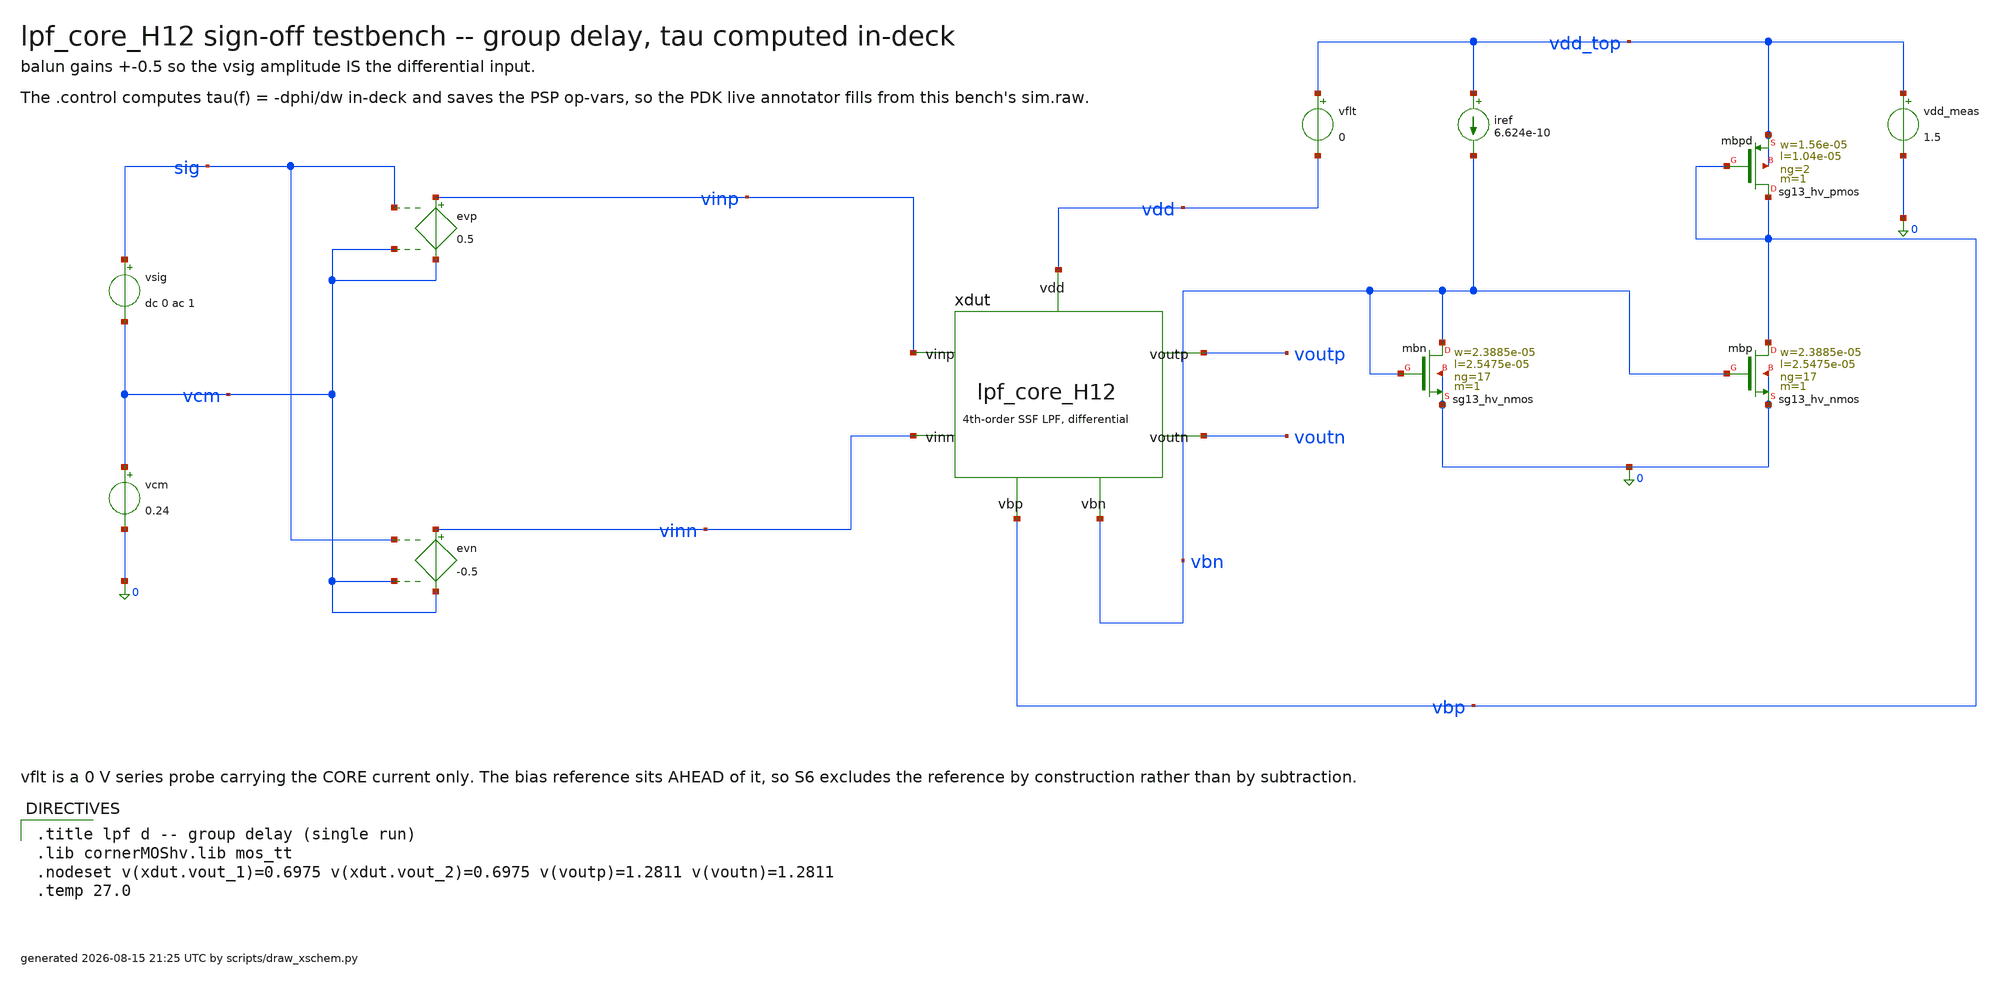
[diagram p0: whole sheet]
** sch_path: signoff/post-pvt/H12-robust/lpf_tb_H12_gd.sch
**.subckt lpf_tb_H12_gd
vsig sig vcm dc 0 ac 1
vcm vcm 0 0.24
evp vinp vcm sig vcm 0.5
evn vinn vcm sig vcm -0.5
xdut vinp vinn voutp voutn vbn vbp vdd lpf_core_H12
vflt vdd_top vdd 0
vdd_meas vdd_top 0 1.5
iref vdd_top vbn 6.624e-10
Xmbn vbn vbn 0 0 sg13_hv_nmos w=2.3885e-05 l=2.5475e-05 ng=17 m=1 mm_ok=1
Xmbp vbp vbn 0 0 sg13_hv_nmos w=2.3885e-05 l=2.5475e-05 ng=17 m=1 mm_ok=1
Xmbpd vbp vbp vdd_top vdd_top sg13_hv_pmos w=1.56e-05 l=1.04e-05 ng=2 m=1 mm_ok=1
**** begin user architecture code

.title lpf d -- group delay (single run)
.lib cornerMOShv.lib mos_tt
.nodeset v(xdut.vout_1)=0.6975 v(xdut.vout_2)=0.6975 v(voutp)=1.2811 v(voutn)=1.2811
.temp 27.0


.control
set filetype=binary
set appendwrite
save all @n.xdut.xm2.nsg13_hv_pmos[ids] @n.xdut.xm2.nsg13_hv_pmos[gm] @n.xdut.xm2.nsg13_hv_pmos[gds]
+ @n.xdut.xm2.nsg13_hv_pmos[gmb] @n.xdut.xm2.nsg13_hv_pmos[vgs] @n.xdut.xm2.nsg13_hv_pmos[vds] @n.xdut.xm2.nsg13_hv_pmos[vth]
+ @n.xdut.xm2.nsg13_hv_pmos[vdss] @n.xdut.xm2.nsg13_hv_pmos[cgg] @n.xdut.xm5.nsg13_hv_pmos[ids] @n.xdut.xm5.nsg13_hv_pmos[gm]
+ @n.xdut.xm5.nsg13_hv_pmos[gds] @n.xdut.xm5.nsg13_hv_pmos[gmb] @n.xdut.xm5.nsg13_hv_pmos[vgs] @n.xdut.xm5.nsg13_hv_pmos[vds]
+ @n.xdut.xm5.nsg13_hv_pmos[vth] @n.xdut.xm5.nsg13_hv_pmos[vdss] @n.xdut.xm5.nsg13_hv_pmos[cgg] @n.xdut.xm4.nsg13_hv_nmos[ids]
+ @n.xdut.xm4.nsg13_hv_nmos[gm] @n.xdut.xm4.nsg13_hv_nmos[gds] @n.xdut.xm4.nsg13_hv_nmos[gmb] @n.xdut.xm4.nsg13_hv_nmos[vgs]
+ @n.xdut.xm4.nsg13_hv_nmos[vds] @n.xdut.xm4.nsg13_hv_nmos[vth] @n.xdut.xm4.nsg13_hv_nmos[vdss] @n.xdut.xm4.nsg13_hv_nmos[cgg]
+ @n.xdut.xm8.nsg13_hv_nmos[ids] @n.xdut.xm8.nsg13_hv_nmos[gm] @n.xdut.xm8.nsg13_hv_nmos[gds] @n.xdut.xm8.nsg13_hv_nmos[gmb]
+ @n.xdut.xm8.nsg13_hv_nmos[vgs] @n.xdut.xm8.nsg13_hv_nmos[vds] @n.xdut.xm8.nsg13_hv_nmos[vth] @n.xdut.xm8.nsg13_hv_nmos[vdss]
+ @n.xdut.xm8.nsg13_hv_nmos[cgg] @n.xdut.xm9.nsg13_hv_nmos[ids] @n.xdut.xm9.nsg13_hv_nmos[gm] @n.xdut.xm9.nsg13_hv_nmos[gds]
+ @n.xdut.xm9.nsg13_hv_nmos[gmb] @n.xdut.xm9.nsg13_hv_nmos[vgs] @n.xdut.xm9.nsg13_hv_nmos[vds] @n.xdut.xm9.nsg13_hv_nmos[vth]
+ @n.xdut.xm9.nsg13_hv_nmos[vdss] @n.xdut.xm9.nsg13_hv_nmos[cgg] @n.xdut.xm10.nsg13_hv_nmos[ids] @n.xdut.xm10.nsg13_hv_nmos[gm]
+ @n.xdut.xm10.nsg13_hv_nmos[gds] @n.xdut.xm10.nsg13_hv_nmos[gmb] @n.xdut.xm10.nsg13_hv_nmos[vgs] @n.xdut.xm10.nsg13_hv_nmos[vds]
+ @n.xdut.xm10.nsg13_hv_nmos[vth] @n.xdut.xm10.nsg13_hv_nmos[vdss] @n.xdut.xm10.nsg13_hv_nmos[cgg] @n.xdut.xmst.nsg13_hv_pmos[ids]
+ @n.xdut.xmst.nsg13_hv_pmos[gm] @n.xdut.xmst.nsg13_hv_pmos[gds] @n.xdut.xmst.nsg13_hv_pmos[gmb] @n.xdut.xmst.nsg13_hv_pmos[vgs]
+ @n.xdut.xmst.nsg13_hv_pmos[vds] @n.xdut.xmst.nsg13_hv_pmos[vth] @n.xdut.xmst.nsg13_hv_pmos[vdss] @n.xdut.xmst.nsg13_hv_pmos[cgg]
+ @n.xdut.xmstn.nsg13_hv_pmos[ids] @n.xdut.xmstn.nsg13_hv_pmos[gm] @n.xdut.xmstn.nsg13_hv_pmos[gds] @n.xdut.xmstn.nsg13_hv_pmos[gmb]
+ @n.xdut.xmstn.nsg13_hv_pmos[vgs] @n.xdut.xmstn.nsg13_hv_pmos[vds] @n.xdut.xmstn.nsg13_hv_pmos[vth] @n.xdut.xmstn.nsg13_hv_pmos[vdss]
+ @n.xdut.xmstn.nsg13_hv_pmos[cgg] @n.xdut.xm0.nsg13_hv_pmos[ids] @n.xdut.xm0.nsg13_hv_pmos[gm] @n.xdut.xm0.nsg13_hv_pmos[gds]
+ @n.xdut.xm0.nsg13_hv_pmos[gmb] @n.xdut.xm0.nsg13_hv_pmos[vgs] @n.xdut.xm0.nsg13_hv_pmos[vds] @n.xdut.xm0.nsg13_hv_pmos[vth]
+ @n.xdut.xm0.nsg13_hv_pmos[vdss] @n.xdut.xm0.nsg13_hv_pmos[cgg] @n.xdut.xm1.nsg13_hv_pmos[ids] @n.xdut.xm1.nsg13_hv_pmos[gm]
+ @n.xdut.xm1.nsg13_hv_pmos[gds] @n.xdut.xm1.nsg13_hv_pmos[gmb] @n.xdut.xm1.nsg13_hv_pmos[vgs] @n.xdut.xm1.nsg13_hv_pmos[vds]
+ @n.xdut.xm1.nsg13_hv_pmos[vth] @n.xdut.xm1.nsg13_hv_pmos[vdss] @n.xdut.xm1.nsg13_hv_pmos[cgg] @n.xdut.xm14.nsg13_hv_pmos[ids]
+ @n.xdut.xm14.nsg13_hv_pmos[gm] @n.xdut.xm14.nsg13_hv_pmos[gds] @n.xdut.xm14.nsg13_hv_pmos[gmb] @n.xdut.xm14.nsg13_hv_pmos[vgs]
+ @n.xdut.xm14.nsg13_hv_pmos[vds] @n.xdut.xm14.nsg13_hv_pmos[vth] @n.xdut.xm14.nsg13_hv_pmos[vdss] @n.xdut.xm14.nsg13_hv_pmos[cgg]
+ @n.xdut.xm15.nsg13_hv_pmos[ids] @n.xdut.xm15.nsg13_hv_pmos[gm] @n.xdut.xm15.nsg13_hv_pmos[gds] @n.xdut.xm15.nsg13_hv_pmos[gmb]
+ @n.xdut.xm15.nsg13_hv_pmos[vgs] @n.xdut.xm15.nsg13_hv_pmos[vds] @n.xdut.xm15.nsg13_hv_pmos[vth] @n.xdut.xm15.nsg13_hv_pmos[vdss]
+ @n.xdut.xm15.nsg13_hv_pmos[cgg] @n.xdut.xr1.nsg13_hv_pmos[ids] @n.xdut.xr1.nsg13_hv_pmos[gm] @n.xdut.xr1.nsg13_hv_pmos[gds]
+ @n.xdut.xr1.nsg13_hv_pmos[gmb] @n.xdut.xr1.nsg13_hv_pmos[vgs] @n.xdut.xr1.nsg13_hv_pmos[vds] @n.xdut.xr1.nsg13_hv_pmos[vth]
+ @n.xdut.xr1.nsg13_hv_pmos[vdss] @n.xdut.xr1.nsg13_hv_pmos[cgg] @n.xdut.xr1.nsg13_hv_pmos[ids] @n.xdut.xr1.nsg13_hv_pmos[gm]
+ @n.xdut.xr1.nsg13_hv_pmos[gds] @n.xdut.xr1.nsg13_hv_pmos[gmb] @n.xdut.xr1.nsg13_hv_pmos[vgs] @n.xdut.xr1.nsg13_hv_pmos[vds]
+ @n.xdut.xr1.nsg13_hv_pmos[vth] @n.xdut.xr1.nsg13_hv_pmos[vdss] @n.xdut.xr1.nsg13_hv_pmos[cgg] @n.xdut.xr2.nsg13_hv_pmos[ids]
+ @n.xdut.xr2.nsg13_hv_pmos[gm] @n.xdut.xr2.nsg13_hv_pmos[gds] @n.xdut.xr2.nsg13_hv_pmos[gmb] @n.xdut.xr2.nsg13_hv_pmos[vgs]
+ @n.xdut.xr2.nsg13_hv_pmos[vds] @n.xdut.xr2.nsg13_hv_pmos[vth] @n.xdut.xr2.nsg13_hv_pmos[vdss] @n.xdut.xr2.nsg13_hv_pmos[cgg]
+ @n.xdut.xr2.nsg13_hv_pmos[ids] @n.xdut.xr2.nsg13_hv_pmos[gm] @n.xdut.xr2.nsg13_hv_pmos[gds] @n.xdut.xr2.nsg13_hv_pmos[gmb]
+ @n.xdut.xr2.nsg13_hv_pmos[vgs] @n.xdut.xr2.nsg13_hv_pmos[vds] @n.xdut.xr2.nsg13_hv_pmos[vth] @n.xdut.xr2.nsg13_hv_pmos[vdss]
+ @n.xdut.xr2.nsg13_hv_pmos[cgg] @n.xdut.xr3.nsg13_hv_nmos[ids] @n.xdut.xr3.nsg13_hv_nmos[gm] @n.xdut.xr3.nsg13_hv_nmos[gds]
+ @n.xdut.xr3.nsg13_hv_nmos[gmb] @n.xdut.xr3.nsg13_hv_nmos[vgs] @n.xdut.xr3.nsg13_hv_nmos[vds] @n.xdut.xr3.nsg13_hv_nmos[vth]
+ @n.xdut.xr3.nsg13_hv_nmos[vdss] @n.xdut.xr3.nsg13_hv_nmos[cgg] @n.xdut.xr3.nsg13_hv_nmos[ids] @n.xdut.xr3.nsg13_hv_nmos[gm]
+ @n.xdut.xr3.nsg13_hv_nmos[gds] @n.xdut.xr3.nsg13_hv_nmos[gmb] @n.xdut.xr3.nsg13_hv_nmos[vgs] @n.xdut.xr3.nsg13_hv_nmos[vds]
+ @n.xdut.xr3.nsg13_hv_nmos[vth] @n.xdut.xr3.nsg13_hv_nmos[vdss] @n.xdut.xr3.nsg13_hv_nmos[cgg]
op
write sim.raw
ac dec 50 0.1 1000
let hdiff = v(voutp) - v(voutn)
let hdb = db(mag(hdiff))
let dc_db = hdb[0]
let ph = cph(hdiff)
let gd = -deriv(ph) / (2 * pi)
let gd_dc_ms = gd[0] * 1e3
let gd_max_ms = vecmax(gd) * 1e3
let hrel = hdb - dc_db
meas ac fc_hz when hrel = -3 fall = 1
print dc_db gd_dc_ms gd_max_ms
write sim.raw hdiff ph gd frequency
.endc

**** end user architecture code
**.ends

* expanding   symbol:  lpf_core_H12.sym # of pins=7
** sym_path: signoff/post-pvt/H12-robust/lpf_core_H12.sym
** sch_path: signoff/post-pvt/H12-robust/lpf_core_H12.sch
.subckt lpf_core_H12 vinp vinn voutp voutn vbn vbp vdd
*.ipin vinp
*.ipin vinn
*.opin voutp
*.opin voutn
*.ipin vdd
*.ipin vbn
*.ipin vbp
Xm2 net2 vinp vout_1 vout_1 sg13_hv_pmos w=1.56e-05 l=1.04e-05 ng=2 m=1 mm_ok=1
Xm5 net3 vinn vout_2 vout_2 sg13_hv_pmos w=1.56e-05 l=1.04e-05 ng=2 m=1 mm_ok=1
Xm4 vout_1 net2 0 0 sg13_hv_nmos w=1.5e-06 l=4.5e-05 ng=1 m=1 mm_ok=1
Xm8 vout_2 net3 0 0 sg13_hv_nmos w=1.5e-06 l=4.5e-05 ng=1 m=1 mm_ok=1
Xm9 net2 vbn 0 0 sg13_hv_nmos w=2.3885e-05 l=2.5475e-05 ng=17 m=1 mm_ok=1
Xm10 net3 vbn 0 0 sg13_hv_nmos w=2.3885e-05 l=2.5475e-05 ng=17 m=1 mm_ok=1
Xmst vout_1 vbr net4 net4 sg13_hv_pmos w=4.86e-06 l=3.276e-05 ng=1 m=1 mm_ok=1
Xmstn vout_2 vbr net1 net1 sg13_hv_pmos w=4.86e-06 l=3.276e-05 ng=1 m=1 mm_ok=1
Xm0 net4 vout_1 voutp voutp sg13_hv_pmos w=4e-06 l=1.5e-05 ng=1 m=1 mm_ok=1
Xm1 net1 vout_2 voutn voutn sg13_hv_pmos w=4e-06 l=1.5e-05 ng=1 m=1 mm_ok=1
Xm14 voutp net4 vdd vdd sg13_hv_pmos w=1.202e-05 l=3.1115e-05 ng=2 m=1 mm_ok=1
Xm15 voutn net1 vdd vdd sg13_hv_pmos w=1.202e-05 l=3.1115e-05 ng=2 m=1 mm_ok=1
Xr1 rep_x rep_x vdd vdd sg13_hv_pmos w=1.202e-05 l=3.1115e-05 ng=2 m=1 mm_ok=1
Xr2 vbr vbr rep_x rep_x sg13_hv_pmos w=4.86e-06 l=3.276e-05 ng=1 m=1 mm_ok=1
Xr3 vbr vbn 0 0 sg13_hv_nmos w=2.3885e-05 l=2.5475e-05 ng=17 m=4 mm_ok=1
c13 net2 vout_1 5.00659e-12 m=1
c17 net3 vout_2 5.00659e-12 m=1
c19 vout_2 vout_1 2.89483e-11 m=1
c1 voutp net4 6.0258e-11 m=1
c10 voutn net1 6.0258e-11 m=1
c12 voutn voutp 2.39864e-11 m=1
.ends

.end
